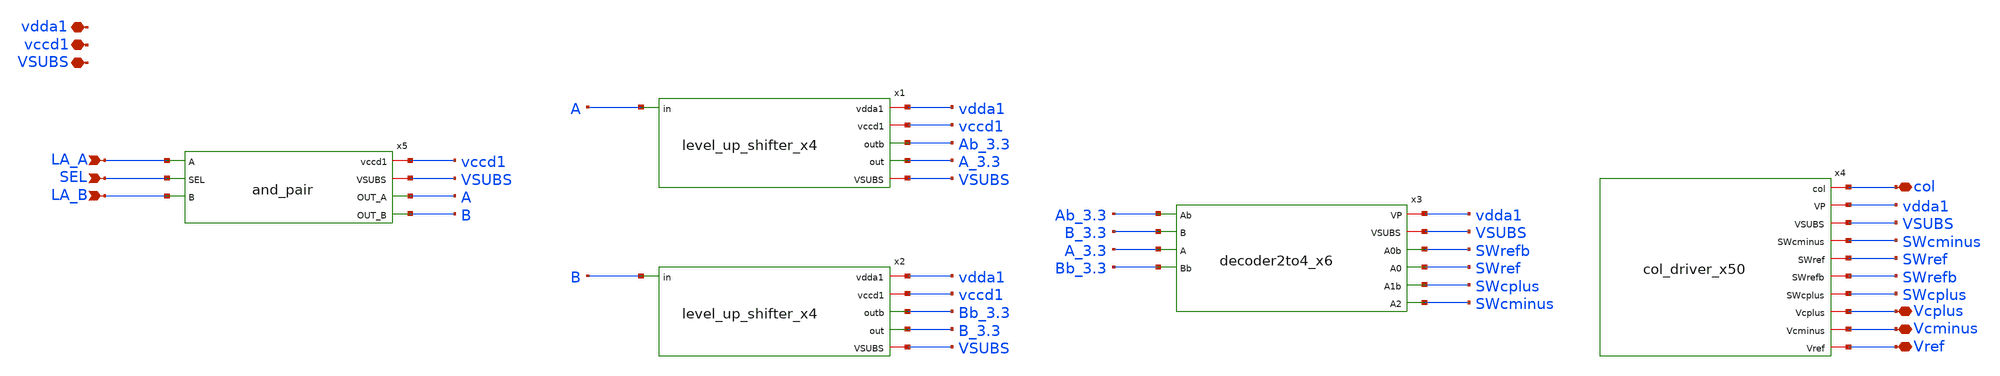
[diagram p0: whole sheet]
** sch_path: xschem/col_driver_big.sch
**.subckt col_driver_big vccd1 vdda1 VSUBS col Vref Vcplus Vcminus LA_A LA_B SEL
*.iopin vccd1
*.iopin vdda1
*.iopin VSUBS
*.iopin col
*.iopin Vref
*.iopin Vcplus
*.iopin Vcminus
*.ipin LA_A
*.ipin LA_B
*.ipin SEL
x1 vdda1 vccd1 A Ab_3.3 A_3.3 VSUBS level_up_shifter_x4
x2 vdda1 vccd1 B Bb_3.3 B_3.3 VSUBS level_up_shifter_x4
x3 vdda1 VSUBS Ab_3.3 SWrefb B_3.3 SWref SWcplus A_3.3 Bb_3.3 SWcminus decoder2to4_x6
x4 col vdda1 VSUBS SWcminus SWref SWrefb SWcplus Vcplus Vcminus Vref col_driver_x50
x5 vccd1 VSUBS LA_A SEL A LA_B B and_pair
**.ends
.end
